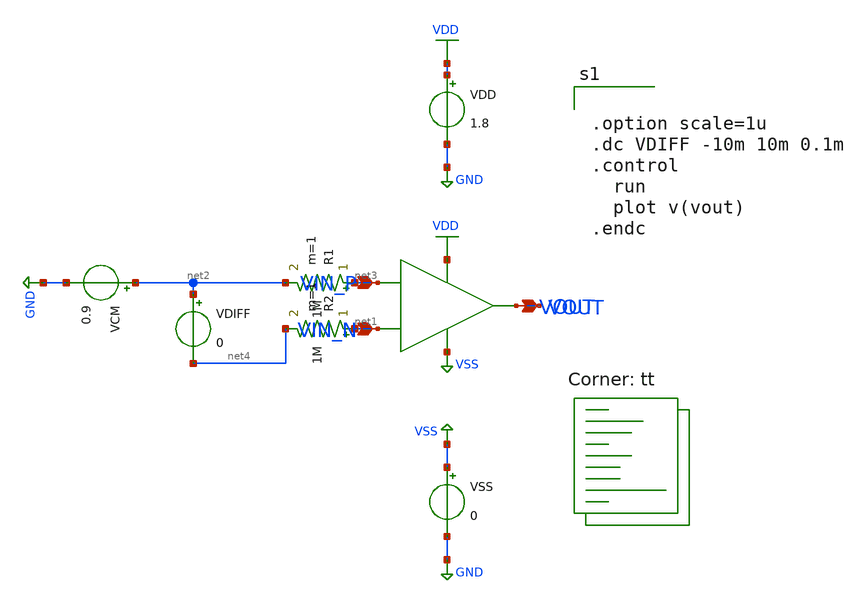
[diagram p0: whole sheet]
** sch_path: analog/schematics/tb_dc_analysis.sch
**.subckt tb_dc_analysis
VDD VDD GND 1.8
VSS VSS GND 0
VCM net2 GND 0.9
R1 net3 net2 1M m=1
R2 net1 net4 1M m=1
VDIFF net2 net4 0
**** begin user architecture code


.option scale=1u
.dc VDIFF -10m 10m 0.1m
.control
  run
  plot v(vout)
.endc


.lib $::SKYWATER_MODELS/sky130.lib.spice tt
**** end user architecture code
**.ends
.GLOBAL VDD
.GLOBAL GND
.GLOBAL VSS
.end
